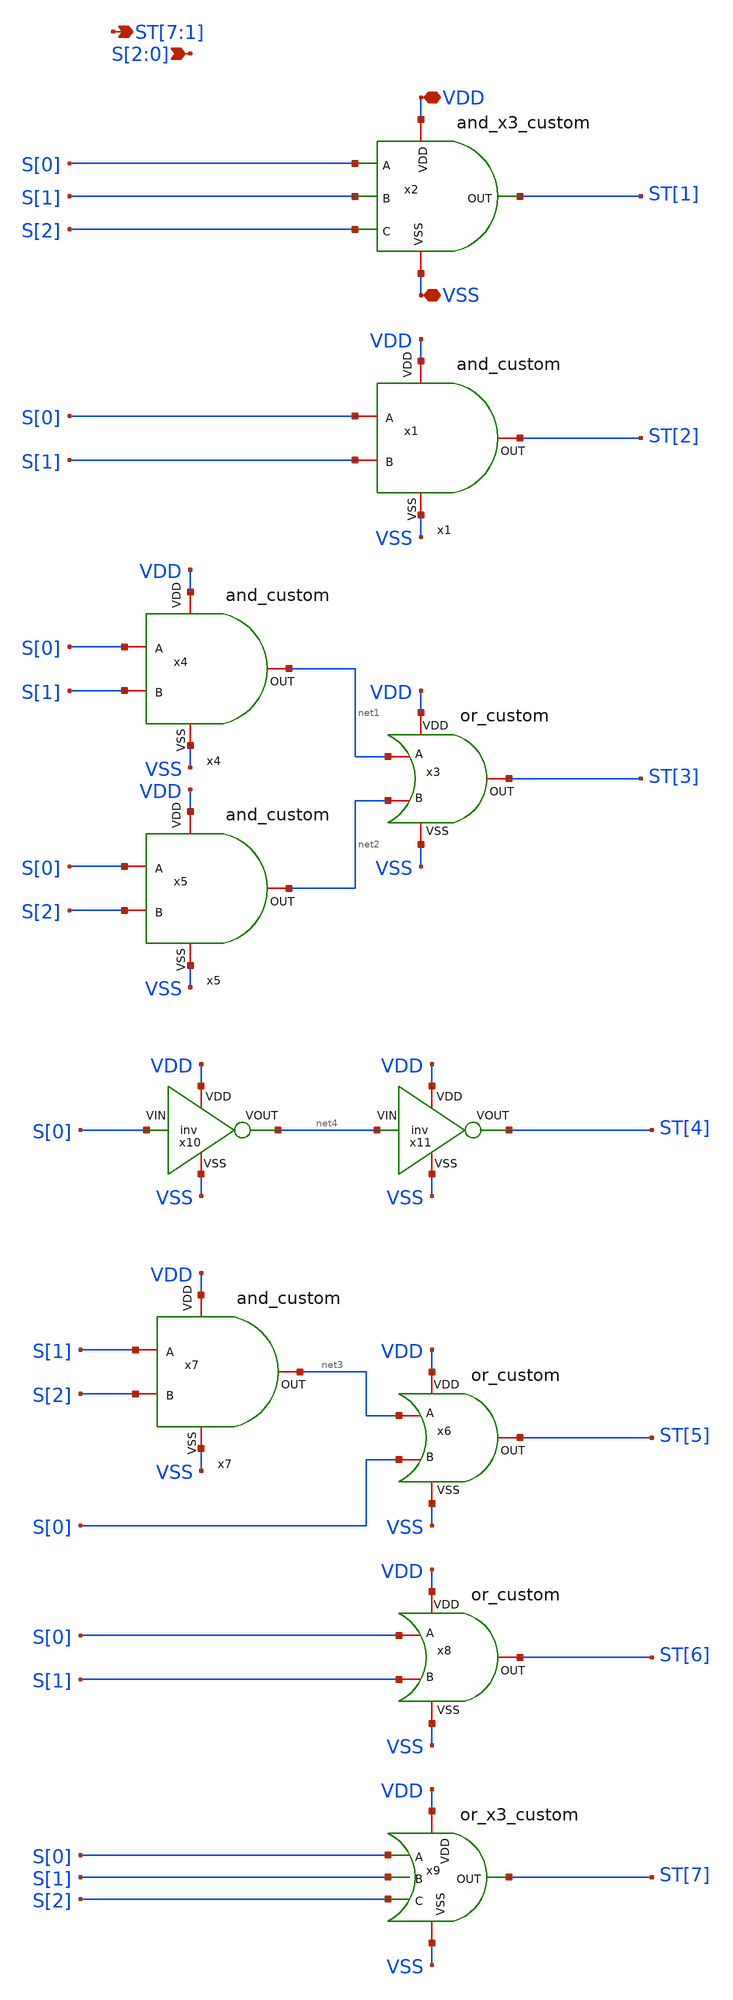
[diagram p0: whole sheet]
** sch_path: design/blocks/3to7_deco/schematic/3to7_deco.sch
**.subckt 3to7_deco VDD VSS ST[7],ST[6],ST[5],ST[4],ST[3],ST[2],ST[1] S[2],S[1],S[0]
*.iopin VDD
*.iopin VSS
*.opin ST[7],ST[6],ST[5],ST[4],ST[3],ST[2],ST[1]
*.ipin S[2],S[1],S[0]
x1 VDD ST[2] S[0] S[1] VSS and_custom
x2 VDD S[0] ST[1] S[1] S[2] VSS and_x3_custom
x3 VDD net1 ST[3] net2 VSS or_custom
x4 VDD net1 S[0] S[1] VSS and_custom
x5 VDD net2 S[0] S[2] VSS and_custom
x6 VDD net3 ST[5] S[0] VSS or_custom
x7 VDD net3 S[1] S[2] VSS and_custom
x8 VDD S[0] ST[6] S[1] VSS or_custom
x9 VDD S[0] ST[7] S[1] S[2] VSS or_x3_custom
x10 VDD net4 S[0] VSS inv
x11 VDD ST[4] net4 VSS inv
**.ends
.end
